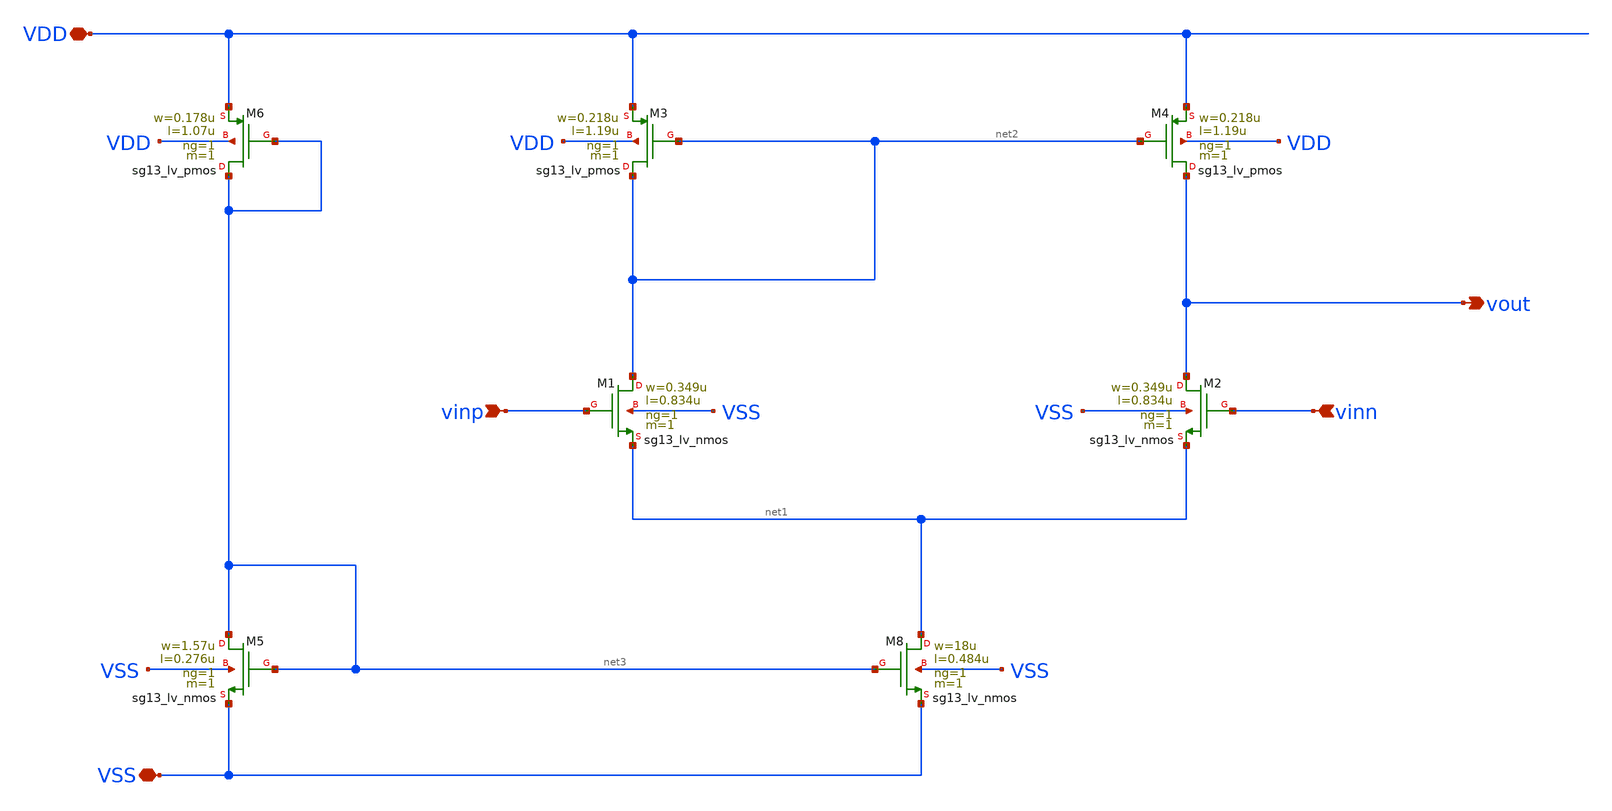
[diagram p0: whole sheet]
** sch_path: analog-db/drawings/shared/amp-single-ended-5t-nmos-input.sch
* Copyright 2026 MacAnalog Research Group
**.subckt amp-single-ended-5t-nmos-input vinp vinn VDD VSS vout
*.ipin vinp
*.ipin vinn
*.iopin VDD
*.iopin VSS
*.opin vout
XM1 net2 vinp net1 VSS sg13_lv_nmos w=0.349u l=0.834u ng=1 m=1 mm_ok=1
XM2 vout vinn net1 VSS sg13_lv_nmos w=0.349u l=0.834u ng=1 m=1 mm_ok=1
XM3 net2 net2 VDD VDD sg13_lv_pmos w=0.218u l=1.19u ng=1 m=1 mm_ok=1
XM4 vout net2 VDD VDD sg13_lv_pmos w=0.218u l=1.19u ng=1 m=1 mm_ok=1
XM8 net1 net3 VSS VSS sg13_lv_nmos w=18u l=0.484u ng=1 m=1 mm_ok=1
XM5 net3 net3 VSS VSS sg13_lv_nmos w=1.57u l=0.276u ng=1 m=1 mm_ok=1
XM6 net3 net3 VDD VDD sg13_lv_pmos w=0.178u l=1.07u ng=1 m=1 mm_ok=1
**.ends
.end
